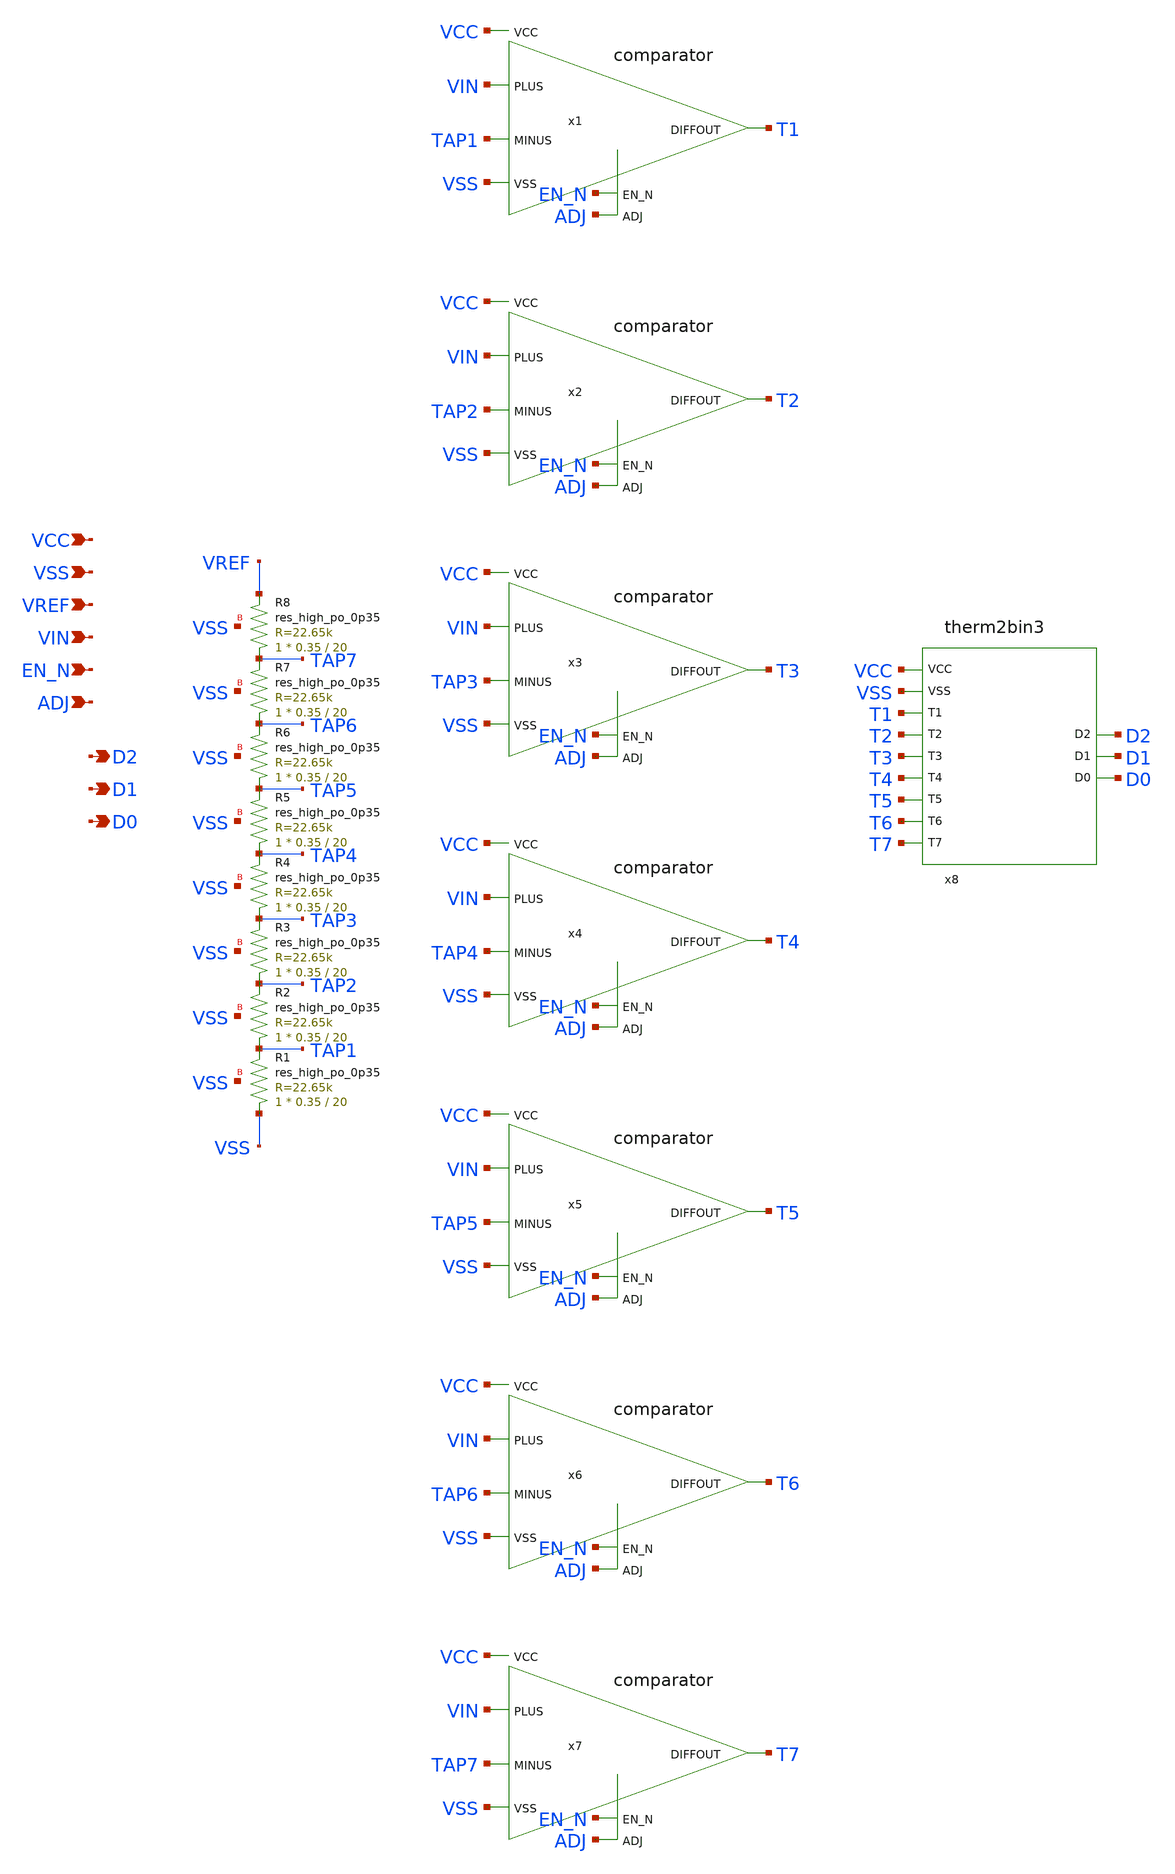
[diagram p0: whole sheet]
** sch_path: flash_adc3.sch
* comparator.sch:
* Copyright 2021 Stefan Frederik Schippers
* Licensed under the Apache License, Version 2.0 (the "License");
**.subckt flash_adc3 VCC VSS VREF VIN EN_N ADJ D2 D1 D0
*.ipin VCC
*.ipin VSS
*.ipin VREF
*.ipin VIN
*.ipin EN_N
*.ipin ADJ
*.opin D2
*.opin D1
*.opin D0
XR8 TAP7 VREF VSS sky130_fd_pr__res_high_po_0p35 L=20 mult=1 m=1
XR7 TAP6 TAP7 VSS sky130_fd_pr__res_high_po_0p35 L=20 mult=1 m=1
XR6 TAP5 TAP6 VSS sky130_fd_pr__res_high_po_0p35 L=20 mult=1 m=1
XR5 TAP4 TAP5 VSS sky130_fd_pr__res_high_po_0p35 L=20 mult=1 m=1
XR4 TAP3 TAP4 VSS sky130_fd_pr__res_high_po_0p35 L=20 mult=1 m=1
XR3 TAP2 TAP3 VSS sky130_fd_pr__res_high_po_0p35 L=20 mult=1 m=1
XR2 TAP1 TAP2 VSS sky130_fd_pr__res_high_po_0p35 L=20 mult=1 m=1
XR1 VSS TAP1 VSS sky130_fd_pr__res_high_po_0p35 L=20 mult=1 m=1
x1 VCC VSS EN_N TAP1 VIN ADJ T1 comparator
x2 VCC VSS EN_N TAP2 VIN ADJ T2 comparator
x3 VCC VSS EN_N TAP3 VIN ADJ T3 comparator
x4 VCC VSS EN_N TAP4 VIN ADJ T4 comparator
x5 VCC VSS EN_N TAP5 VIN ADJ T5 comparator
x6 VCC VSS EN_N TAP6 VIN ADJ T6 comparator
x7 VCC VSS EN_N TAP7 VIN ADJ T7 comparator
x8 VCC VSS T1 T2 T3 T4 T5 T6 T7 D2 D1 D0 therm2bin3
**.ends

* expanding   symbol:  /home/ttuser/Documents/ADCAnalogDesign/comparator.sym # of pins=7
** sym_path: comparator.sym
** sch_path: comparator.sch
.subckt comparator VCC VSS EN_N MINUS PLUS ADJ DIFFOUT
*.ipin VCC
*.ipin VSS
*.ipin EN_N
*.ipin MINUS
*.ipin PLUS
*.ipin ADJ
*.opin DIFFOUT
XM3 net1 EN_N VCC VCC sky130_fd_pr__pfet_01v8 L=8 W=1 nf=1 ad='int((nf+1)/2) * W/nf * 0.29' as='int((nf+2)/2) * W/nf * 0.29'
+ pd='2*int((nf+1)/2) * (W/nf + 0.29)' ps='2*int((nf+2)/2) * (W/nf + 0.29)' nrd='0.29 / W' nrs='0.29 / W'
+ sa=0 sb=0 sd=0 mult=1 m=1
XM7 Inhigh EN_N VCC VCC sky130_fd_pr__pfet_01v8 L=8 W=2 nf=1 ad='int((nf+1)/2) * W/nf * 0.29' as='int((nf+2)/2) * W/nf * 0.29'
+ pd='2*int((nf+1)/2) * (W/nf + 0.29)' ps='2*int((nf+2)/2) * (W/nf + 0.29)' nrd='0.29 / W' nrs='0.29 / W'
+ sa=0 sb=0 sd=0 mult=1 m=1
XM16 mirhigh EN_N VCC VCC sky130_fd_pr__pfet_01v8 L=0.15 W=5 nf=1 ad='int((nf+1)/2) * W/nf * 0.29' as='int((nf+2)/2) * W/nf * 0.29'
+ pd='2*int((nf+1)/2) * (W/nf + 0.29)' ps='2*int((nf+2)/2) * (W/nf + 0.29)' nrd='0.29 / W' nrs='0.29 / W'
+ sa=0 sb=0 sd=0 mult=1 m=1
XM4 G1 ADJ net1 VCC sky130_fd_pr__pfet_01v8_lvt L=1 W=1 nf=1 ad='int((nf+1)/2) * W/nf * 0.29' as='int((nf+2)/2) * W/nf * 0.29'
+ pd='2*int((nf+1)/2) * (W/nf + 0.29)' ps='2*int((nf+2)/2) * (W/nf + 0.29)' nrd='0.29 / W' nrs='0.29 / W'
+ sa=0 sb=0 sd=0 mult=1 m=1
XM5 G1 ADJ net2 VSS sky130_fd_pr__nfet_01v8_lvt L=1 W=0.5 nf=1 ad='int((nf+1)/2) * W/nf * 0.29' as='int((nf+2)/2) * W/nf * 0.29'
+ pd='2*int((nf+1)/2) * (W/nf + 0.29)' ps='2*int((nf+2)/2) * (W/nf + 0.29)' nrd='0.29 / W' nrs='0.29 / W'
+ sa=0 sb=0 sd=0 mult=1 m=1
XM6 net2 VCC VSS VSS sky130_fd_pr__nfet_01v8_lvt L=8 W=0.5 nf=1 ad='int((nf+1)/2) * W/nf * 0.29' as='int((nf+2)/2) * W/nf * 0.29'
+ pd='2*int((nf+1)/2) * (W/nf + 0.29)' ps='2*int((nf+2)/2) * (W/nf + 0.29)' nrd='0.29 / W' nrs='0.29 / W'
+ sa=0 sb=0 sd=0 mult=1 m=1
XM9 G1 MINUS Inhigh VCC sky130_fd_pr__pfet_01v8_lvt L=2 W=8 nf=1 ad='int((nf+1)/2) * W/nf * 0.29' as='int((nf+2)/2) * W/nf * 0.29'
+ pd='2*int((nf+1)/2) * (W/nf + 0.29)' ps='2*int((nf+2)/2) * (W/nf + 0.29)' nrd='0.29 / W' nrs='0.29 / W'
+ sa=0 sb=0 sd=0 mult=1 m=1
XM8 G2 PLUS Inhigh VCC sky130_fd_pr__pfet_01v8_lvt L=2 W=8 nf=1 ad='int((nf+1)/2) * W/nf * 0.29' as='int((nf+2)/2) * W/nf * 0.29'
+ pd='2*int((nf+1)/2) * (W/nf + 0.29)' ps='2*int((nf+2)/2) * (W/nf + 0.29)' nrd='0.29 / W' nrs='0.29 / W'
+ sa=0 sb=0 sd=0 mult=1 m=1
XM11 G2 G2 VSS VSS sky130_fd_pr__nfet_01v8_lvt L=4 W=2 nf=1 ad='int((nf+1)/2) * W/nf * 0.29' as='int((nf+2)/2) * W/nf * 0.29'
+ pd='2*int((nf+1)/2) * (W/nf + 0.29)' ps='2*int((nf+2)/2) * (W/nf + 0.29)' nrd='0.29 / W' nrs='0.29 / W'
+ sa=0 sb=0 sd=0 mult=1 m=1
XM10 G1 G1 VSS VSS sky130_fd_pr__nfet_01v8_lvt L=4 W=2 nf=1 ad='int((nf+1)/2) * W/nf * 0.29' as='int((nf+2)/2) * W/nf * 0.29'
+ pd='2*int((nf+1)/2) * (W/nf + 0.29)' ps='2*int((nf+2)/2) * (W/nf + 0.29)' nrd='0.29 / W' nrs='0.29 / W'
+ sa=0 sb=0 sd=0 mult=1 m=1
XM12 DIFFOUT G2 VSS VSS sky130_fd_pr__nfet_01v8_lvt L=4 W=2 nf=1 ad='int((nf+1)/2) * W/nf * 0.29' as='int((nf+2)/2) * W/nf * 0.29'
+ pd='2*int((nf+1)/2) * (W/nf + 0.29)' ps='2*int((nf+2)/2) * (W/nf + 0.29)' nrd='0.29 / W' nrs='0.29 / W'
+ sa=0 sb=0 sd=0 mult=1 m=1
XM13 DIFFOUT EN_N VSS VSS sky130_fd_pr__nfet_01v8_lvt L=0.15 W=1 nf=1 ad='int((nf+1)/2) * W/nf * 0.29'
+ as='int((nf+2)/2) * W/nf * 0.29' pd='2*int((nf+1)/2) * (W/nf + 0.29)' ps='2*int((nf+2)/2) * (W/nf + 0.29)'
+ nrd='0.29 / W' nrs='0.29 / W' sa=0 sb=0 sd=0 mult=1 m=1
XM17 pg2g G1 VSS VSS sky130_fd_pr__nfet_01v8_lvt L=4 W=2 nf=1 ad='int((nf+1)/2) * W/nf * 0.29' as='int((nf+2)/2) * W/nf * 0.29'
+ pd='2*int((nf+1)/2) * (W/nf + 0.29)' ps='2*int((nf+2)/2) * (W/nf + 0.29)' nrd='0.29 / W' nrs='0.29 / W'
+ sa=0 sb=0 sd=0 mult=1 m=1
XM15 pg2g pg2g mirhigh VCC sky130_fd_pr__pfet_01v8_lvt L=4 W=4 nf=1 ad='int((nf+1)/2) * W/nf * 0.29'
+ as='int((nf+2)/2) * W/nf * 0.29' pd='2*int((nf+1)/2) * (W/nf + 0.29)' ps='2*int((nf+2)/2) * (W/nf + 0.29)'
+ nrd='0.29 / W' nrs='0.29 / W' sa=0 sb=0 sd=0 mult=1 m=1
XM2 DIFFOUT pg2g mirhigh VCC sky130_fd_pr__pfet_01v8_lvt L=4 W=4 nf=1 ad='int((nf+1)/2) * W/nf * 0.29'
+ as='int((nf+2)/2) * W/nf * 0.29' pd='2*int((nf+1)/2) * (W/nf + 0.29)' ps='2*int((nf+2)/2) * (W/nf + 0.29)'
+ nrd='0.29 / W' nrs='0.29 / W' sa=0 sb=0 sd=0 mult=1 m=1
.ends


* expanding   symbol:  /home/ttuser/Documents/ADCAnalogDesign/therm2bin3.sym # of pins=12
** sym_path: therm2bin3.sym
** sch_path: therm2bin3.sch
.subckt therm2bin3 VCC VSS T1 T2 T3 T4 T5 T6 T7 D2 D1 D0
*.ipin VCC
*.ipin VSS
*.ipin T1
*.ipin T2
*.ipin T3
*.ipin T4
*.ipin T5
*.ipin T6
*.ipin T7
*.opin D2
*.opin D1
*.opin D0
x3 VCC T6 T6B VSS inverter
x5 T1 T2B N1 VCC VSS nand2
x6 T3 T4B N2 VCC VSS nand2
x7 T5 T6B N3 VCC VSS nand2
x8 T2 T4B N4 VCC VSS nand2
x9 VCC T4B D2 VSS inverter
x10 T6B N4 D1 VCC VSS nand2
x11 VCC VSS N1 N2 N3 T7B D0 nand4
x1 VCC T7 T7B VSS inverter
x2 VCC T2 T2B VSS inverter
x4 VCC T4 T4B VSS inverter
.ends


* expanding   symbol:  /home/ttuser/Documents/ADCAnalogDesign/inverter.sym # of pins=4
** sym_path: inverter.sym
** sch_path: inverter.sch
.subckt inverter VDD IN out VSS
*.ipin IN
*.opin out
*.iopin VDD
*.iopin VSS
XM3 out IN VDD VDD sky130_fd_pr__pfet_01v8 L=0.15 W=1 nf=1 ad='int((nf+1)/2) * W/nf * 0.29' as='int((nf+2)/2) * W/nf * 0.29'
+ pd='2*int((nf+1)/2) * (W/nf + 0.29)' ps='2*int((nf+2)/2) * (W/nf + 0.29)' nrd='0.29 / W' nrs='0.29 / W'
+ sa=0 sb=0 sd=0 mult=1 m=1
XM2 out IN VSS VSS sky130_fd_pr__nfet_01v8 L=0.15 W=1 nf=1 ad='int((nf+1)/2) * W/nf * 0.29' as='int((nf+2)/2) * W/nf * 0.29'
+ pd='2*int((nf+1)/2) * (W/nf + 0.29)' ps='2*int((nf+2)/2) * (W/nf + 0.29)' nrd='0.29 / W' nrs='0.29 / W'
+ sa=0 sb=0 sd=0 mult=1 m=1
.ends


* expanding   symbol:  /home/ttuser/Documents/ADCAnalogDesign/nand2.sym # of pins=5
** sym_path: nand2.sym
** sch_path: nand2.sch
.subckt nand2 A B Y VCC VSS
*.ipin A
*.ipin B
*.opin Y
*.iopin VCC
*.iopin VSS
XM1 Y A VCC VCC sky130_fd_pr__pfet_01v8 L=0.15 W=2 nf=1 ad='int((nf+1)/2) * W/nf * 0.29' as='int((nf+2)/2) * W/nf * 0.29'
+ pd='2*int((nf+1)/2) * (W/nf + 0.29)' ps='2*int((nf+2)/2) * (W/nf + 0.29)' nrd='0.29 / W' nrs='0.29 / W'
+ sa=0 sb=0 sd=0 mult=1 m=1
XM2 Y B VCC VCC sky130_fd_pr__pfet_01v8 L=0.15 W=2 nf=1 ad='int((nf+1)/2) * W/nf * 0.29' as='int((nf+2)/2) * W/nf * 0.29'
+ pd='2*int((nf+1)/2) * (W/nf + 0.29)' ps='2*int((nf+2)/2) * (W/nf + 0.29)' nrd='0.29 / W' nrs='0.29 / W'
+ sa=0 sb=0 sd=0 mult=1 m=1
XM3 Y A N1 VSS sky130_fd_pr__nfet_01v8 L=0.15 W=2 nf=1 ad='int((nf+1)/2) * W/nf * 0.29' as='int((nf+2)/2) * W/nf * 0.29'
+ pd='2*int((nf+1)/2) * (W/nf + 0.29)' ps='2*int((nf+2)/2) * (W/nf + 0.29)' nrd='0.29 / W' nrs='0.29 / W'
+ sa=0 sb=0 sd=0 mult=1 m=1
XM4 N1 B VSS VSS sky130_fd_pr__nfet_01v8 L=0.15 W=2 nf=1 ad='int((nf+1)/2) * W/nf * 0.29' as='int((nf+2)/2) * W/nf * 0.29'
+ pd='2*int((nf+1)/2) * (W/nf + 0.29)' ps='2*int((nf+2)/2) * (W/nf + 0.29)' nrd='0.29 / W' nrs='0.29 / W'
+ sa=0 sb=0 sd=0 mult=1 m=1
.ends


* expanding   symbol:  /home/ttuser/Documents/ADCAnalogDesign/nand4.sym # of pins=7
** sym_path: nand4.sym
** sch_path: nand4.sch
.subckt nand4 VCC VSS A B C D Y
*.ipin VCC
*.ipin VSS
*.ipin A
*.ipin B
*.ipin C
*.ipin D
*.opin Y
XM1 Y A VCC VCC sky130_fd_pr__pfet_01v8 L=0.15 W=2 nf=1 ad='int((nf+1)/2) * W/nf * 0.29' as='int((nf+2)/2) * W/nf * 0.29'
+ pd='2*int((nf+1)/2) * (W/nf + 0.29)' ps='2*int((nf+2)/2) * (W/nf + 0.29)' nrd='0.29 / W' nrs='0.29 / W'
+ sa=0 sb=0 sd=0 mult=1 m=1
XM2 Y B VCC VCC sky130_fd_pr__pfet_01v8 L=0.15 W=2 nf=1 ad='int((nf+1)/2) * W/nf * 0.29' as='int((nf+2)/2) * W/nf * 0.29'
+ pd='2*int((nf+1)/2) * (W/nf + 0.29)' ps='2*int((nf+2)/2) * (W/nf + 0.29)' nrd='0.29 / W' nrs='0.29 / W'
+ sa=0 sb=0 sd=0 mult=1 m=1
XM3 Y C VCC VCC sky130_fd_pr__pfet_01v8 L=0.15 W=2 nf=1 ad='int((nf+1)/2) * W/nf * 0.29' as='int((nf+2)/2) * W/nf * 0.29'
+ pd='2*int((nf+1)/2) * (W/nf + 0.29)' ps='2*int((nf+2)/2) * (W/nf + 0.29)' nrd='0.29 / W' nrs='0.29 / W'
+ sa=0 sb=0 sd=0 mult=1 m=1
XM4 Y D VCC VCC sky130_fd_pr__pfet_01v8 L=0.15 W=2 nf=1 ad='int((nf+1)/2) * W/nf * 0.29' as='int((nf+2)/2) * W/nf * 0.29'
+ pd='2*int((nf+1)/2) * (W/nf + 0.29)' ps='2*int((nf+2)/2) * (W/nf + 0.29)' nrd='0.29 / W' nrs='0.29 / W'
+ sa=0 sb=0 sd=0 mult=1 m=1
XM5 Y A n1 VSS sky130_fd_pr__nfet_01v8 L=0.15 W=4 nf=1 ad='int((nf+1)/2) * W/nf * 0.29' as='int((nf+2)/2) * W/nf * 0.29'
+ pd='2*int((nf+1)/2) * (W/nf + 0.29)' ps='2*int((nf+2)/2) * (W/nf + 0.29)' nrd='0.29 / W' nrs='0.29 / W'
+ sa=0 sb=0 sd=0 mult=1 m=1
XM6 n1 B n2 VSS sky130_fd_pr__nfet_01v8 L=0.15 W=4 nf=1 ad='int((nf+1)/2) * W/nf * 0.29' as='int((nf+2)/2) * W/nf * 0.29'
+ pd='2*int((nf+1)/2) * (W/nf + 0.29)' ps='2*int((nf+2)/2) * (W/nf + 0.29)' nrd='0.29 / W' nrs='0.29 / W'
+ sa=0 sb=0 sd=0 mult=1 m=1
XM7 n2 C n3 VSS sky130_fd_pr__nfet_01v8 L=0.15 W=4 nf=1 ad='int((nf+1)/2) * W/nf * 0.29' as='int((nf+2)/2) * W/nf * 0.29'
+ pd='2*int((nf+1)/2) * (W/nf + 0.29)' ps='2*int((nf+2)/2) * (W/nf + 0.29)' nrd='0.29 / W' nrs='0.29 / W'
+ sa=0 sb=0 sd=0 mult=1 m=1
XM8 n3 D VSS VSS sky130_fd_pr__nfet_01v8 L=0.15 W=4 nf=1 ad='int((nf+1)/2) * W/nf * 0.29' as='int((nf+2)/2) * W/nf * 0.29'
+ pd='2*int((nf+1)/2) * (W/nf + 0.29)' ps='2*int((nf+2)/2) * (W/nf + 0.29)' nrd='0.29 / W' nrs='0.29 / W'
+ sa=0 sb=0 sd=0 mult=1 m=1
.ends

.end
